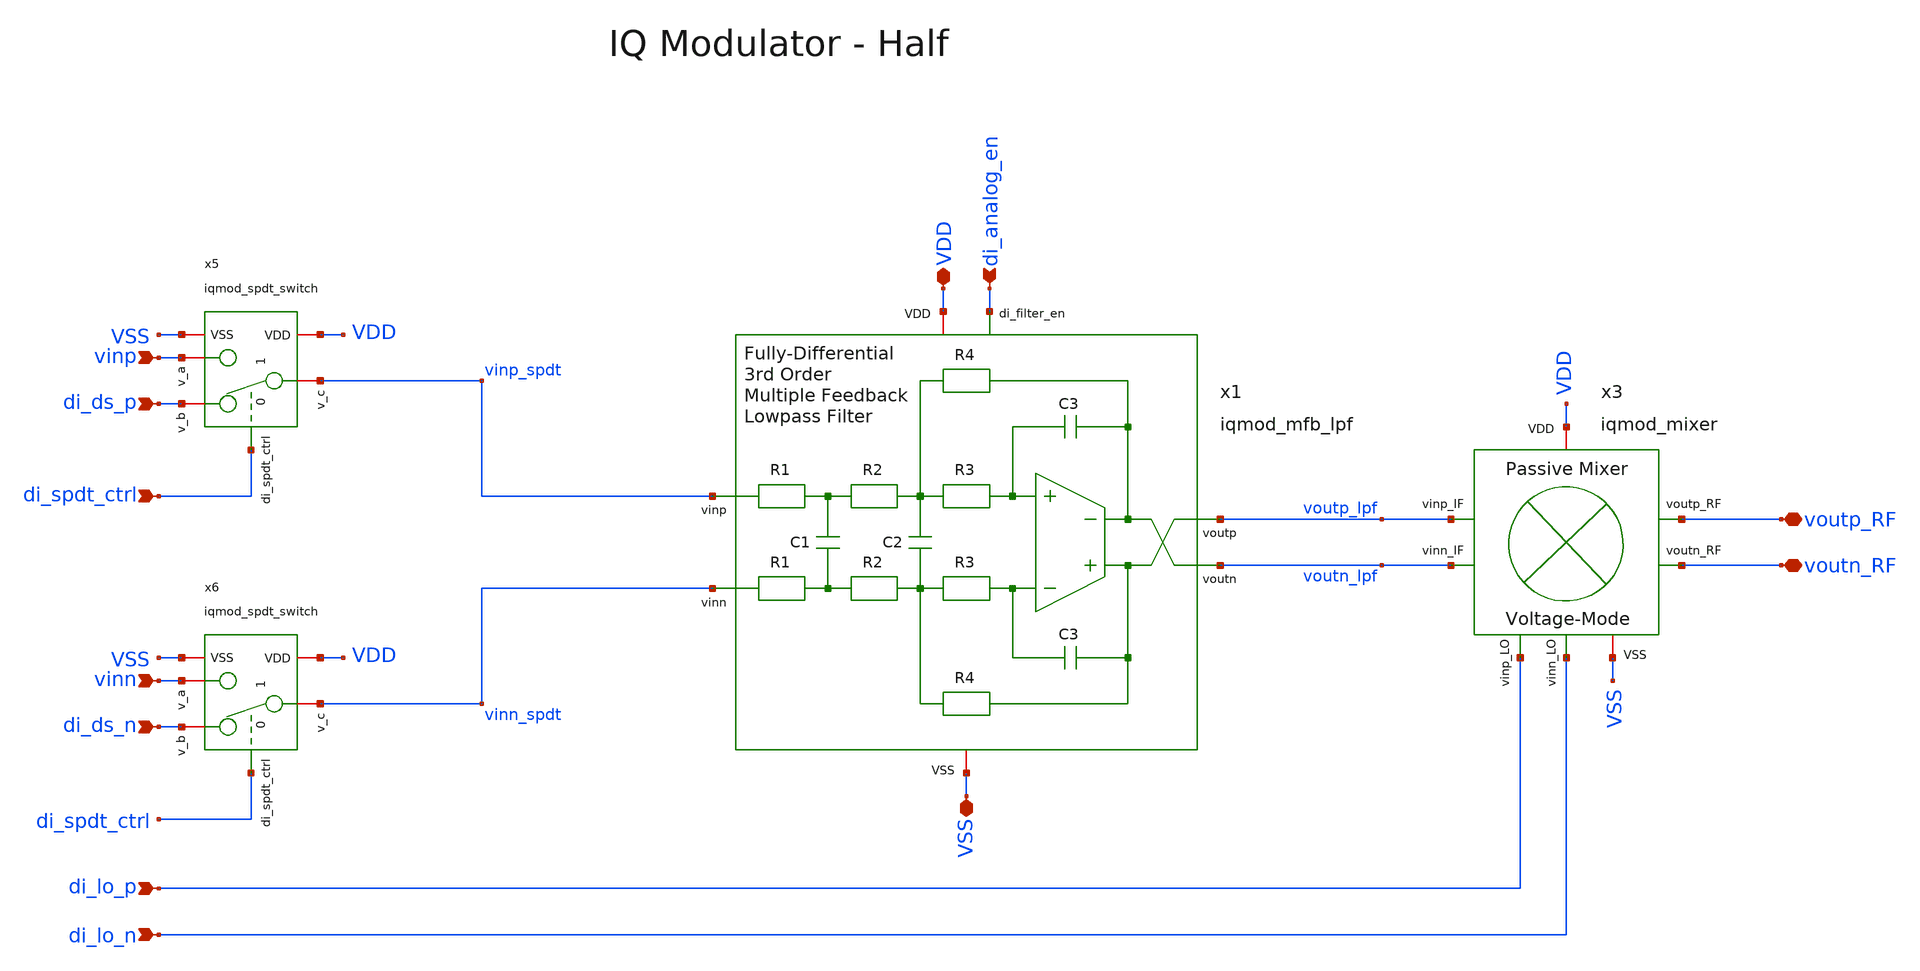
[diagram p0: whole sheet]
** sch_path: ihp130/macros/iqmod/schematic/xschem/iqmod_top_half.sch
**.subckt iqmod_top_half VDD voutp_RF VSS di_lo_p di_lo_n di_ds_p voutn_RF di_analog_en vinp vinn
*+ di_spdt_ctrl di_ds_n
*.iopin VDD
*.iopin voutp_RF
*.iopin VSS
*.ipin di_lo_p
*.ipin di_lo_n
*.ipin di_ds_p
*.iopin voutn_RF
*.ipin di_analog_en
*.ipin vinp
*.ipin vinn
*.ipin di_spdt_ctrl
*.ipin di_ds_n
x3 voutp_lpf voutn_lpf voutp_RF di_lo_p di_lo_n VDD VSS voutn_RF iqmod_mixer
x1 voutp_lpf vinp_spdt voutn_lpf vinn_spdt VDD VSS di_analog_en iqmod_mfb_lpf
x5 VDD di_spdt_ctrl VSS vinp_spdt di_ds_p vinp iqmod_spdt_switch
x6 VDD di_spdt_ctrl VSS vinn_spdt di_ds_n vinn iqmod_spdt_switch
**.ends
.end
